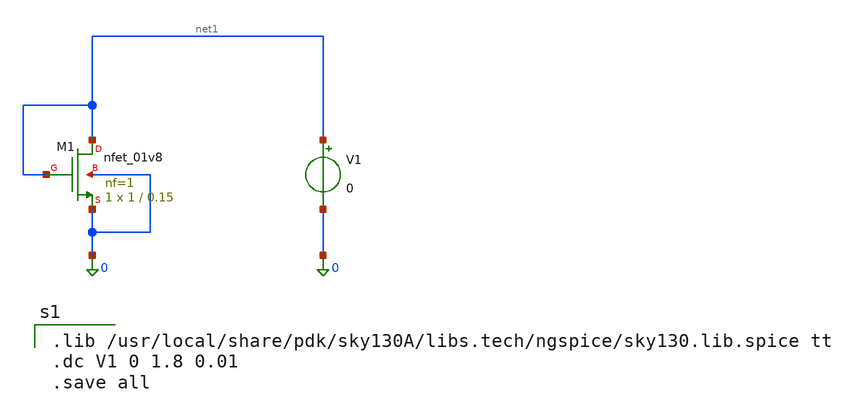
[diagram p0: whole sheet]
** sch_path: nmos_as_a_diode/nmos_diode.sch
**.subckt nmos_diode
XM1 net1 net1 0 0 sky130_fd_pr__nfet_01v8 L=0.15 W=1 nf=1 ad='int((1 + 1)/2) * 1 / 1 * 0.29' as='int((1 + 2)/2) * 1 / 1 * 0.29'
+ pd='2*int((1 + 1)/2) * (1 / 1 + 0.29)' ps='2*int((1 + 2)/2) * (1 / 1 + 0.29)' nrd='0.29 / 1 ' nrs='0.29 / 1 '
+ sa=0 sb=0 sd=0 mult=1 m=1
V1 net1 0 0
**** begin user architecture code

.lib /usr/local/share/pdk/sky130A/libs.tech/ngspice/sky130.lib.spice tt
.dc V1 0 1.8 0.01
.save all

**** end user architecture code
**.ends
.end
